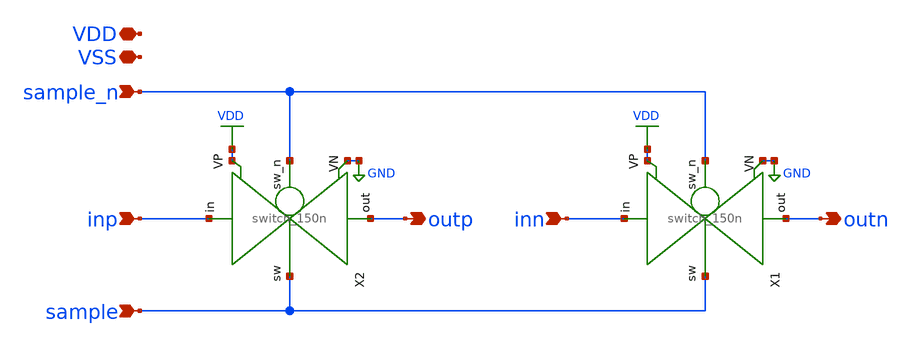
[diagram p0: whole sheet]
** sch_path: xschem/adc_sample_switch/adc_sample_switch.sch
* xschem/switch/switch_150n.sch:
* Copyright 2022 Manuel Moser
* Licensed under the Apache License, Version 2.0 (the "License");
**.subckt adc_sample_switch inp inn outp outn sample sample_n VSS VDD
*.ipin inp
*.ipin inn
*.opin outp
*.opin outn
*.ipin sample
*.ipin sample_n
*.iopin VSS
*.iopin VDD
X1 sample_n inn sample outn VDD GND switch_150n
X2 sample_n inp sample outp VDD GND switch_150n
**.ends

* expanding   symbol:  /foss/designs/SKY130_SAR-ADC/xschem/switch_150n/switch_150n.sym # of pins=6
** sym_path: xschem/switch/switch_150n.sym
** sch_path: xschem/switch/switch_150n.sch
.subckt switch_150n sw_n in sw out VP VN
*.iopin VN
*.iopin VP
*.ipin IN
*.opin OUT
*.ipin SW_N
*.ipin SW
XM2 IN SW OUT VN sky130_fd_pr__nfet_01v8_lvt L=0.35 W=2 nf=1 ad='int((nf+1)/2) * W/nf * 0.29' as='int((nf+2)/2) * W/nf * 0.29'
+ pd='2*int((nf+1)/2) * (W/nf + 0.29)' ps='2*int((nf+2)/2) * (W/nf + 0.29)' nrd='0.29 / W' nrs='0.29 / W'
+ sa=0 sb=0 sd=0 mult=1 m=1
XM1 IN SW_N OUT VP sky130_fd_pr__pfet_01v8 L=0.15 W=1.7 nf=1 ad='int((nf+1)/2) * W/nf * 0.29' as='int((nf+2)/2) * W/nf * 0.29'
+ pd='2*int((nf+1)/2) * (W/nf + 0.29)' ps='2*int((nf+2)/2) * (W/nf + 0.29)' nrd='0.29 / W' nrs='0.29 / W'
+ sa=0 sb=0 sd=0 mult=1 m=1
.ends

.GLOBAL VDD
.GLOBAL GND
.end
